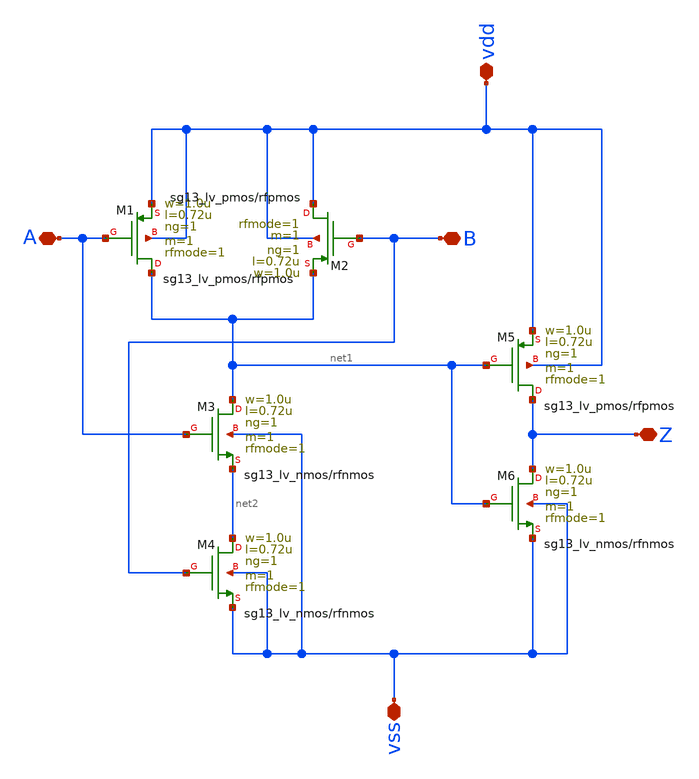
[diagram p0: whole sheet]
** sch_path: design/blocks/andgate/schematic/andgate.sch
**.subckt andgate A vdd vss B Z
*.iopin A
*.iopin vdd
*.iopin vss
*.iopin B
*.iopin Z
XM1 net1 A vdd vdd sg13_lv_pmos w=1.0u l=0.72u ng=1 m=1 rfmode=1 mm_ok=1
XM2 vdd B net1 vdd sg13_lv_pmos w=1.0u l=0.72u ng=1 m=1 rfmode=1 mm_ok=1
XM3 net1 A net2 vss sg13_lv_nmos w=1.0u l=0.72u ng=1 m=1 rfmode=1 mm_ok=1
XM4 net2 B vss vss sg13_lv_nmos w=1.0u l=0.72u ng=1 m=1 rfmode=1 mm_ok=1
XM5 Z net1 vdd vdd sg13_lv_pmos w=1.0u l=0.72u ng=1 m=1 rfmode=1 mm_ok=1
XM6 Z net1 vss vss sg13_lv_nmos w=1.0u l=0.72u ng=1 m=1 rfmode=1 mm_ok=1
**.ends
.end
